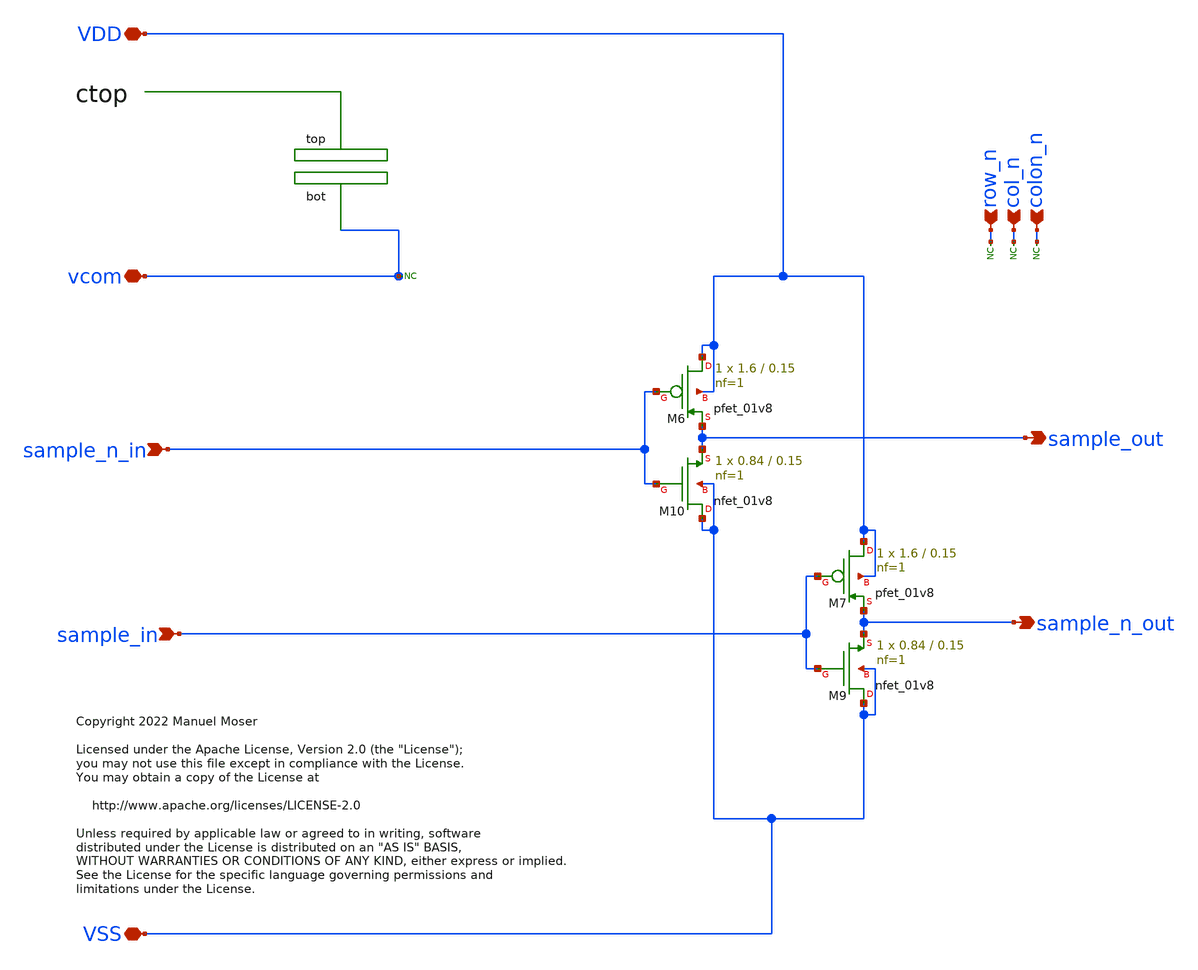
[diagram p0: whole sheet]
** sch_path: xschem/adc_array_circuit_150n/adc_array_circuit_150n_drv.sch
* Copyright 2022 Manuel Moser
* Licensed under the Apache License, Version 2.0 (the "License");
**.subckt adc_array_circuit_150n_drv sample_n_in sample_in vcom row_n col_n colon_n VDD VSS
*+ sample_out sample_n_out
*.ipin sample_n_in
*.ipin sample_in
*.iopin vcom
*.ipin row_n
*.ipin col_n
*.ipin colon_n
*.iopin VDD
*.iopin VSS
*.opin sample_out
*.opin sample_n_out
XM6 VDD sample_n_in sample_out VDD sky130_fd_pr__pfet_01v8 L=0.15 W=1.6 nf=1 ad='int((nf+1)/2) * W/nf * 0.29'
+ as='int((nf+2)/2) * W/nf * 0.29' pd='2*int((nf+1)/2) * (W/nf + 0.29)' ps='2*int((nf+2)/2) * (W/nf + 0.29)'
+ nrd='0.29 / W' nrs='0.29 / W' sa=0 sb=0 sd=0 mult=1 m=1
XM7 VDD sample_in sample_n_out VDD sky130_fd_pr__pfet_01v8 L=0.15 W=1.6 nf=1 ad='int((nf+1)/2) * W/nf * 0.29'
+ as='int((nf+2)/2) * W/nf * 0.29' pd='2*int((nf+1)/2) * (W/nf + 0.29)' ps='2*int((nf+2)/2) * (W/nf + 0.29)'
+ nrd='0.29 / W' nrs='0.29 / W' sa=0 sb=0 sd=0 mult=1 m=1
XM9 VSS sample_in sample_n_out VSS sky130_fd_pr__nfet_01v8 L=0.15 W=0.84 nf=1 ad='int((nf+1)/2) * W/nf * 0.29'
+ as='int((nf+2)/2) * W/nf * 0.29' pd='2*int((nf+1)/2) * (W/nf + 0.29)' ps='2*int((nf+2)/2) * (W/nf + 0.29)'
+ nrd='0.29 / W' nrs='0.29 / W' sa=0 sb=0 sd=0 mult=1 m=1
XM10 VSS sample_n_in sample_out VSS sky130_fd_pr__nfet_01v8 L=0.15 W=0.84 nf=1 ad='int((nf+1)/2) * W/nf * 0.29'
+ as='int((nf+2)/2) * W/nf * 0.29' pd='2*int((nf+1)/2) * (W/nf + 0.29)' ps='2*int((nf+2)/2) * (W/nf + 0.29)'
+ nrd='0.29 / W' nrs='0.29 / W' sa=0 sb=0 sd=0 mult=1 m=1
* noconn row_n
* noconn col_n
* noconn colon_n
* noconn vcom
**.ends
.end
